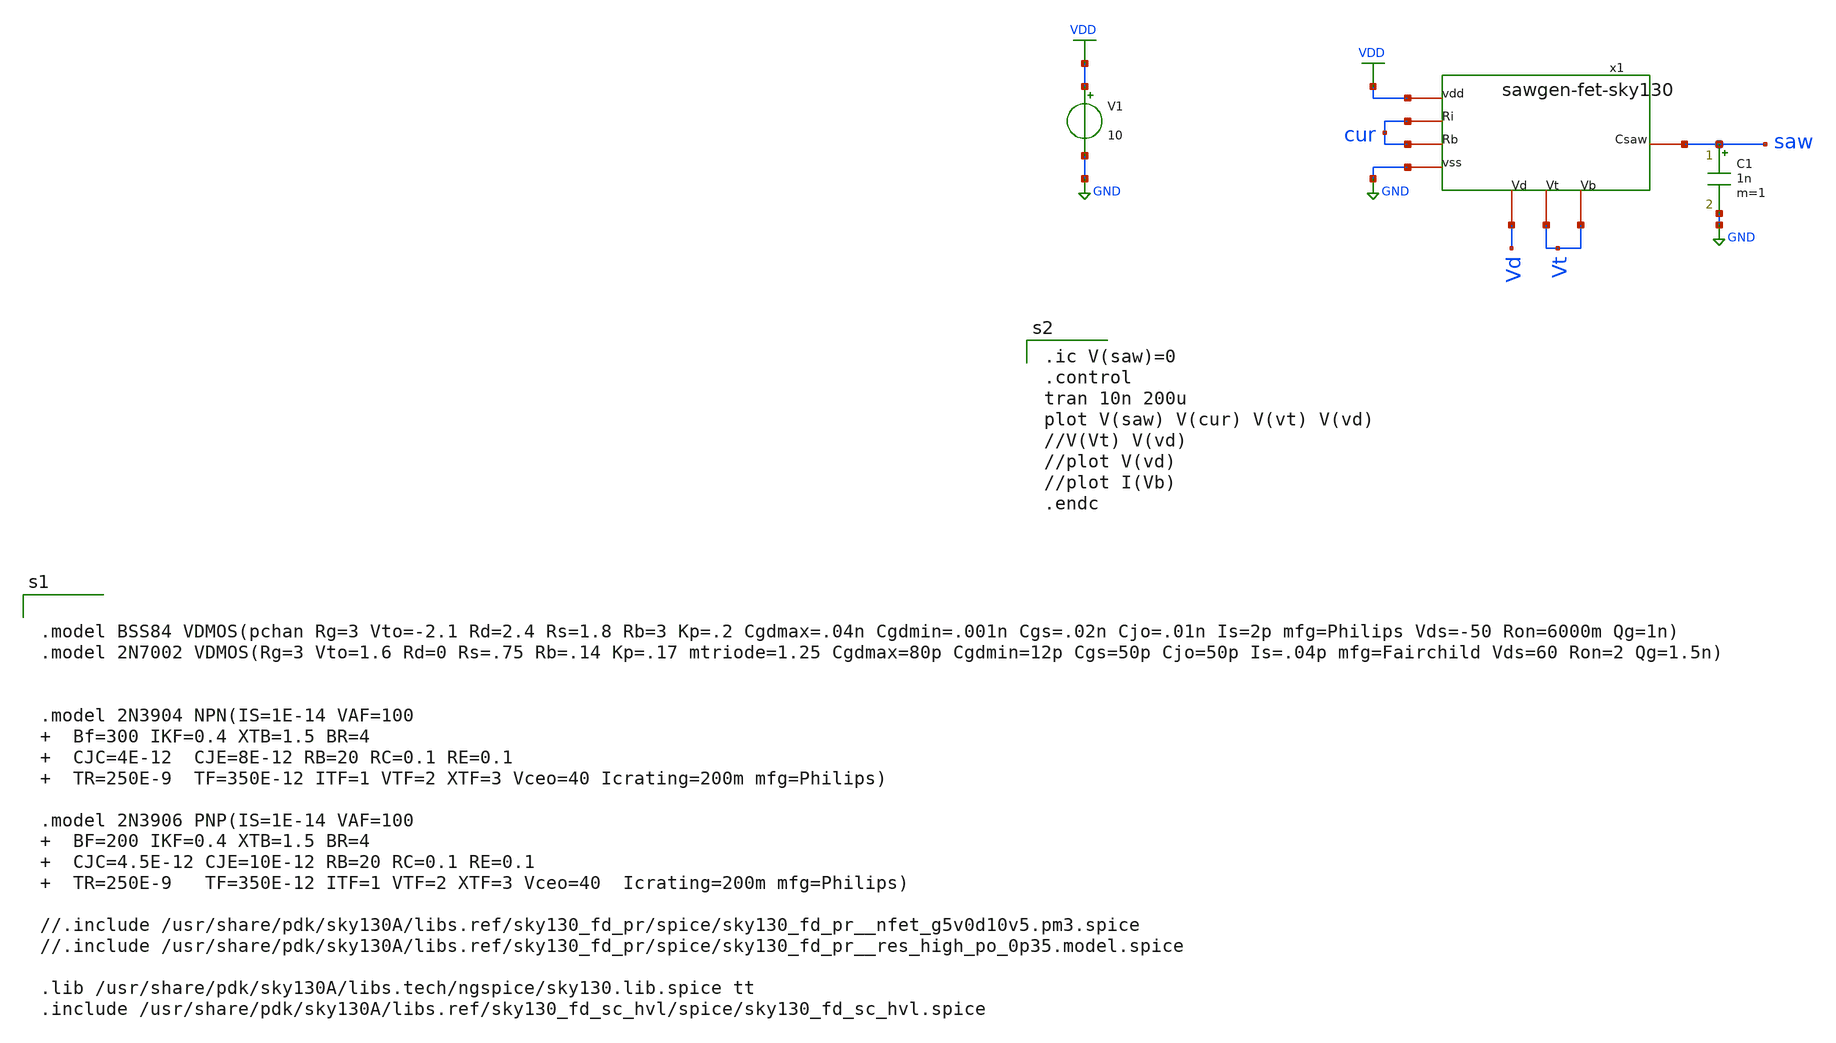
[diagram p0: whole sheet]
** sch_path: xschem/sawgen-fet-sky130_tb.sch
**.subckt sawgen-fet-sky130_tb
V1 VDD GND 10
x1 VDD cur cur GND Vd Vt Vt saw sawgen-fet-sky130
C1 saw GND 1n m=1
**** begin user architecture code


.model BSS84 VDMOS(pchan Rg=3 Vto=-2.1 Rd=2.4 Rs=1.8 Rb=3 Kp=.2 Cgdmax=.04n Cgdmin=.001n Cgs=.02n
+ Cjo=.01n Is=2p mfg=Philips Vds=-50 Ron=6000m Qg=1n)
.model 2N7002 VDMOS(Rg=3 Vto=1.6 Rd=0 Rs=.75 Rb=.14 Kp=.17 mtriode=1.25 Cgdmax=80p Cgdmin=12p
+ Cgs=50p Cjo=50p Is=.04p mfg=Fairchild Vds=60 Ron=2 Qg=1.5n)


.model 2N3904 NPN(IS=1E-14 VAF=100   Bf=300 IKF=0.4 XTB=1.5 BR=4   CJC=4E-12  CJE=8E-12 RB=20 RC=0.1
+ RE=0.1   TR=250E-9  TF=350E-12 ITF=1 VTF=2 XTF=3 Vceo=40 Icrating=200m mfg=Philips)

.model 2N3906 PNP(IS=1E-14 VAF=100   BF=200 IKF=0.4 XTB=1.5 BR=4   CJC=4.5E-12 CJE=10E-12 RB=20
+ RC=0.1 RE=0.1   TR=250E-9   TF=350E-12 ITF=1 VTF=2 XTF=3 Vceo=40  Icrating=200m mfg=Philips)

//.include /usr/share/pdk/sky130A/libs.ref/sky130_fd_pr/spice/sky130_fd_pr__nfet_g5v0d10v5.pm3.spice
//.include /usr/share/pdk/sky130A/libs.ref/sky130_fd_pr/spice/sky130_fd_pr__res_high_po_0p35.model.spice

.lib /usr/share/pdk/sky130A/libs.tech/ngspice/sky130.lib.spice tt
.include /usr/share/pdk/sky130A/libs.ref/sky130_fd_sc_hvl/spice/sky130_fd_sc_hvl.spice


.ic V(saw)=0
.control
tran 10n 200u
plot V(saw) V(cur) V(vt) V(vd)
//V(Vt) V(vd)
//plot V(vd)
//plot I(Vb)
.endc

**** end user architecture code
**.ends

* expanding   symbol:  sawgen-fet-sky130.sym # of pins=8
** sym_path: xschem/sawgen-fet-sky130.sym
** sch_path: xschem/sawgen-fet-sky130.sch
.subckt sawgen-fet-sky130 vdd Ri Rb vss Vd vt vb Csaw
*.ipin VDD
*.ipin VSS
*.iopin Rb
*.iopin Ri
*.iopin Csaw
*.iopin Vt
*.iopin Vb
*.iopin Vd
XM5 Ri Ri VDD VDD sky130_fd_pr__pfet_g5v0d10v5 L=0.8 W=16 nf=1 ad='int((nf+1)/2) * W/nf * 0.29' as='int((nf+2)/2) * W/nf * 0.29'
+ pd='2*int((nf+1)/2) * (W/nf + 0.29)' ps='2*int((nf+2)/2) * (W/nf + 0.29)' nrd='0.29 / W' nrs='0.29 / W'
+ sa=0 sb=0 sd=0 mult=1 m=1
XM6 Csaw Ri VDD VDD sky130_fd_pr__pfet_g5v0d10v5 L=0.8 W=2 nf=1 ad='int((nf+1)/2) * W/nf * 0.29' as='int((nf+2)/2) * W/nf * 0.29'
+ pd='2*int((nf+1)/2) * (W/nf + 0.29)' ps='2*int((nf+2)/2) * (W/nf + 0.29)' nrd='0.29 / W' nrs='0.29 / W'
+ sa=0 sb=0 sd=0 mult=1 m=1
XR8 VSS Rb VSS sky130_fd_pr__res_high_po_0p35 L=20 mult=1 m=1
XM1 Vd Vt Csaw VDD sky130_fd_pr__pfet_g5v0d10v5 L=0.8 W=16 nf=1 ad='int((nf+1)/2) * W/nf * 0.29' as='int((nf+2)/2) * W/nf * 0.29'
+ pd='2*int((nf+1)/2) * (W/nf + 0.29)' ps='2*int((nf+2)/2) * (W/nf + 0.29)' nrd='0.29 / W' nrs='0.29 / W'
+ sa=0 sb=0 sd=0 mult=1 m=1
XR3 Vb VDD VSS sky130_fd_pr__res_high_po_0p35 L=20 mult=1 m=1
XR4 VSS Vb VSS sky130_fd_pr__res_high_po_0p35 L=20 mult=1 m=1
XM4 Vt Vd VSS VSS sky130_fd_pr__nfet_g5v0d10v5 L=0.8 W=2 nf=1 ad='int((nf+1)/2) * W/nf * 0.29' as='int((nf+2)/2) * W/nf * 0.29'
+ pd='2*int((nf+1)/2) * (W/nf + 0.29)' ps='2*int((nf+2)/2) * (W/nf + 0.29)' nrd='0.29 / W' nrs='0.29 / W'
+ sa=0 sb=0 sd=0 mult=1 m=1
XM2 Vd Vd VSS VSS sky130_fd_pr__nfet_g5v0d10v5 L=0.8 W=2 nf=1 ad='int((nf+1)/2) * W/nf * 0.29' as='int((nf+2)/2) * W/nf * 0.29'
+ pd='2*int((nf+1)/2) * (W/nf + 0.29)' ps='2*int((nf+2)/2) * (W/nf + 0.29)' nrd='0.29 / W' nrs='0.29 / W'
+ sa=0 sb=0 sd=0 mult=1 m=1
.ends

.GLOBAL VDD
.GLOBAL GND
.end
